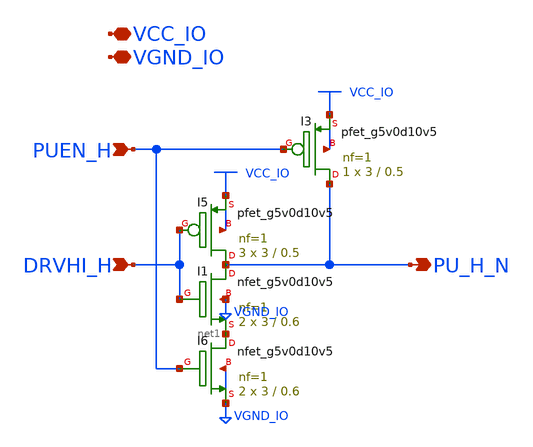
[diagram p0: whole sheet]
** sch_path: com_pupredrvr_strong_slow.sch
* Copyright 2023 David Mitchell Bailey
* Licensed under the Apache License, Version 2.0 (the "License");
* you may not use this file except in compliance with the License.
* You may obtain a copy of the License at
* https://www.apache.org/licenses/LICENSE-2.0
* Unless required by applicable law or agreed to in writing, software
* distributed under the License is distributed on an "AS IS" BASIS,
* WITHOUT WARRANTIES OR CONDITIONS OF ANY KIND, either express or implied.
* See the License for the specific language governing permissions and
* limitations under the License.
**.subckt com_pupredrvr_strong_slow DRVHI_H PU_H_N VCC_IO VGND_IO PUEN_H
*.ipin DRVHI_H
*.opin PU_H_N
*.iopin VCC_IO
*.iopin VGND_IO
*.ipin PUEN_H
XI1 PU_H_N DRVHI_H net1 VGND_IO sky130_fd_pr__nfet_g5v0d10v5 L=0.6 W=3 nf=1 ad='int((nf+1)/2) * W/nf * 0.29'
+ as='int((nf+2)/2) * W/nf * 0.29' pd='2*int((nf+1)/2) * (W/nf + 0.29)' ps='2*int((nf+2)/2) * (W/nf + 0.29)'
+ nrd='0.29 / W' nrs='0.29 / W' sa=0 sb=0 sd=0 mult=2 m=2
XI5 PU_H_N DRVHI_H VCC_IO VCC_IO sky130_fd_pr__pfet_g5v0d10v5 L=0.5 W=3 nf=1 ad='int((nf+1)/2) * W/nf * 0.29'
+ as='int((nf+2)/2) * W/nf * 0.29' pd='2*int((nf+1)/2) * (W/nf + 0.29)' ps='2*int((nf+2)/2) * (W/nf + 0.29)'
+ nrd='0.29 / W' nrs='0.29 / W' sa=0 sb=0 sd=0 mult=3 m=3
XI3 PU_H_N PUEN_H VCC_IO VCC_IO sky130_fd_pr__pfet_g5v0d10v5 L=0.5 W=3 nf=1 ad='int((nf+1)/2) * W/nf * 0.29'
+ as='int((nf+2)/2) * W/nf * 0.29' pd='2*int((nf+1)/2) * (W/nf + 0.29)' ps='2*int((nf+2)/2) * (W/nf + 0.29)'
+ nrd='0.29 / W' nrs='0.29 / W' sa=0 sb=0 sd=0 mult=1 m=1
XI6 net1 PUEN_H VGND_IO VGND_IO sky130_fd_pr__nfet_g5v0d10v5 L=0.6 W=3 nf=1 ad='int((nf+1)/2) * W/nf * 0.29'
+ as='int((nf+2)/2) * W/nf * 0.29' pd='2*int((nf+1)/2) * (W/nf + 0.29)' ps='2*int((nf+2)/2) * (W/nf + 0.29)'
+ nrd='0.29 / W' nrs='0.29 / W' sa=0 sb=0 sd=0 mult=2 m=2
**.ends
.end
